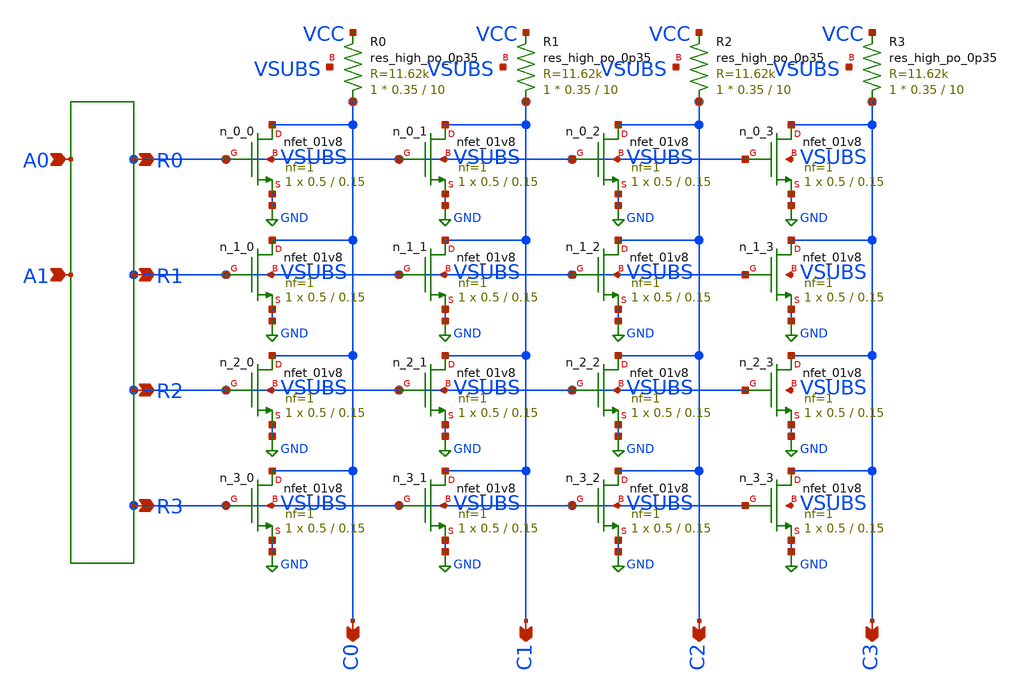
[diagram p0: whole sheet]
** sch_path: xschem/rom_4x4.sch
**.subckt rom_4x4 C0 C1 C2 C3
*.opin C0
*.opin C1
*.opin C2
*.opin C3
XR0 C0 VCC VSUBS sky130_fd_pr__res_high_po_0p35 L=10 mult=1 m=1
XR1 C1 VCC VSUBS sky130_fd_pr__res_high_po_0p35 L=10 mult=1 m=1
XR2 C2 VCC VSUBS sky130_fd_pr__res_high_po_0p35 L=10 mult=1 m=1
XR3 C3 VCC VSUBS sky130_fd_pr__res_high_po_0p35 L=10 mult=1 m=1
Xn_0_0 C0 VSUBS GND VSUBS sky130_fd_pr__nfet_01v8 L=0.15 W=0.5 nf=1 ad='int((1 + 1)/2) * 0.5 / 1 * 0.29'
+ as='int((1 + 2)/2) * 0.5 / 1 * 0.29' pd='2*int((1 + 1)/2) * (0.5 / 1 + 0.29)' ps='2*int((1 + 2)/2) * (0.5 / 1 + 0.29)'
+ nrd='0.29 / 0.5 ' nrs='0.29 / 0.5 ' sa=0 sb=0 sd=0 mult=1 m=1
Xn_0_1 C1 VSUBS GND VSUBS sky130_fd_pr__nfet_01v8 L=0.15 W=0.5 nf=1 ad='int((1 + 1)/2) * 0.5 / 1 * 0.29'
+ as='int((1 + 2)/2) * 0.5 / 1 * 0.29' pd='2*int((1 + 1)/2) * (0.5 / 1 + 0.29)' ps='2*int((1 + 2)/2) * (0.5 / 1 + 0.29)'
+ nrd='0.29 / 0.5 ' nrs='0.29 / 0.5 ' sa=0 sb=0 sd=0 mult=1 m=1
Xn_0_2 C2 VSUBS GND VSUBS sky130_fd_pr__nfet_01v8 L=0.15 W=0.5 nf=1 ad='int((1 + 1)/2) * 0.5 / 1 * 0.29'
+ as='int((1 + 2)/2) * 0.5 / 1 * 0.29' pd='2*int((1 + 1)/2) * (0.5 / 1 + 0.29)' ps='2*int((1 + 2)/2) * (0.5 / 1 + 0.29)'
+ nrd='0.29 / 0.5 ' nrs='0.29 / 0.5 ' sa=0 sb=0 sd=0 mult=1 m=1
Xn_0_3 C3 VSUBS GND VSUBS sky130_fd_pr__nfet_01v8 L=0.15 W=0.5 nf=1 ad='int((1 + 1)/2) * 0.5 / 1 * 0.29'
+ as='int((1 + 2)/2) * 0.5 / 1 * 0.29' pd='2*int((1 + 1)/2) * (0.5 / 1 + 0.29)' ps='2*int((1 + 2)/2) * (0.5 / 1 + 0.29)'
+ nrd='0.29 / 0.5 ' nrs='0.29 / 0.5 ' sa=0 sb=0 sd=0 mult=1 m=1
Xn_1_0 C0 VSUBS GND VSUBS sky130_fd_pr__nfet_01v8 L=0.15 W=0.5 nf=1 ad='int((1 + 1)/2) * 0.5 / 1 * 0.29'
+ as='int((1 + 2)/2) * 0.5 / 1 * 0.29' pd='2*int((1 + 1)/2) * (0.5 / 1 + 0.29)' ps='2*int((1 + 2)/2) * (0.5 / 1 + 0.29)'
+ nrd='0.29 / 0.5 ' nrs='0.29 / 0.5 ' sa=0 sb=0 sd=0 mult=1 m=1
Xn_1_1 C1 VSUBS GND VSUBS sky130_fd_pr__nfet_01v8 L=0.15 W=0.5 nf=1 ad='int((1 + 1)/2) * 0.5 / 1 * 0.29'
+ as='int((1 + 2)/2) * 0.5 / 1 * 0.29' pd='2*int((1 + 1)/2) * (0.5 / 1 + 0.29)' ps='2*int((1 + 2)/2) * (0.5 / 1 + 0.29)'
+ nrd='0.29 / 0.5 ' nrs='0.29 / 0.5 ' sa=0 sb=0 sd=0 mult=1 m=1
Xn_1_2 C2 VSUBS GND VSUBS sky130_fd_pr__nfet_01v8 L=0.15 W=0.5 nf=1 ad='int((1 + 1)/2) * 0.5 / 1 * 0.29'
+ as='int((1 + 2)/2) * 0.5 / 1 * 0.29' pd='2*int((1 + 1)/2) * (0.5 / 1 + 0.29)' ps='2*int((1 + 2)/2) * (0.5 / 1 + 0.29)'
+ nrd='0.29 / 0.5 ' nrs='0.29 / 0.5 ' sa=0 sb=0 sd=0 mult=1 m=1
Xn_1_3 C3 VSUBS GND VSUBS sky130_fd_pr__nfet_01v8 L=0.15 W=0.5 nf=1 ad='int((1 + 1)/2) * 0.5 / 1 * 0.29'
+ as='int((1 + 2)/2) * 0.5 / 1 * 0.29' pd='2*int((1 + 1)/2) * (0.5 / 1 + 0.29)' ps='2*int((1 + 2)/2) * (0.5 / 1 + 0.29)'
+ nrd='0.29 / 0.5 ' nrs='0.29 / 0.5 ' sa=0 sb=0 sd=0 mult=1 m=1
Xn_2_0 C0 VSUBS GND VSUBS sky130_fd_pr__nfet_01v8 L=0.15 W=0.5 nf=1 ad='int((1 + 1)/2) * 0.5 / 1 * 0.29'
+ as='int((1 + 2)/2) * 0.5 / 1 * 0.29' pd='2*int((1 + 1)/2) * (0.5 / 1 + 0.29)' ps='2*int((1 + 2)/2) * (0.5 / 1 + 0.29)'
+ nrd='0.29 / 0.5 ' nrs='0.29 / 0.5 ' sa=0 sb=0 sd=0 mult=1 m=1
Xn_2_1 C1 VSUBS GND VSUBS sky130_fd_pr__nfet_01v8 L=0.15 W=0.5 nf=1 ad='int((1 + 1)/2) * 0.5 / 1 * 0.29'
+ as='int((1 + 2)/2) * 0.5 / 1 * 0.29' pd='2*int((1 + 1)/2) * (0.5 / 1 + 0.29)' ps='2*int((1 + 2)/2) * (0.5 / 1 + 0.29)'
+ nrd='0.29 / 0.5 ' nrs='0.29 / 0.5 ' sa=0 sb=0 sd=0 mult=1 m=1
Xn_2_2 C2 VSUBS GND VSUBS sky130_fd_pr__nfet_01v8 L=0.15 W=0.5 nf=1 ad='int((1 + 1)/2) * 0.5 / 1 * 0.29'
+ as='int((1 + 2)/2) * 0.5 / 1 * 0.29' pd='2*int((1 + 1)/2) * (0.5 / 1 + 0.29)' ps='2*int((1 + 2)/2) * (0.5 / 1 + 0.29)'
+ nrd='0.29 / 0.5 ' nrs='0.29 / 0.5 ' sa=0 sb=0 sd=0 mult=1 m=1
Xn_2_3 C3 VSUBS GND VSUBS sky130_fd_pr__nfet_01v8 L=0.15 W=0.5 nf=1 ad='int((1 + 1)/2) * 0.5 / 1 * 0.29'
+ as='int((1 + 2)/2) * 0.5 / 1 * 0.29' pd='2*int((1 + 1)/2) * (0.5 / 1 + 0.29)' ps='2*int((1 + 2)/2) * (0.5 / 1 + 0.29)'
+ nrd='0.29 / 0.5 ' nrs='0.29 / 0.5 ' sa=0 sb=0 sd=0 mult=1 m=1
Xn_3_0 C0 VSUBS GND VSUBS sky130_fd_pr__nfet_01v8 L=0.15 W=0.5 nf=1 ad='int((1 + 1)/2) * 0.5 / 1 * 0.29'
+ as='int((1 + 2)/2) * 0.5 / 1 * 0.29' pd='2*int((1 + 1)/2) * (0.5 / 1 + 0.29)' ps='2*int((1 + 2)/2) * (0.5 / 1 + 0.29)'
+ nrd='0.29 / 0.5 ' nrs='0.29 / 0.5 ' sa=0 sb=0 sd=0 mult=1 m=1
Xn_3_1 C1 VSUBS GND VSUBS sky130_fd_pr__nfet_01v8 L=0.15 W=0.5 nf=1 ad='int((1 + 1)/2) * 0.5 / 1 * 0.29'
+ as='int((1 + 2)/2) * 0.5 / 1 * 0.29' pd='2*int((1 + 1)/2) * (0.5 / 1 + 0.29)' ps='2*int((1 + 2)/2) * (0.5 / 1 + 0.29)'
+ nrd='0.29 / 0.5 ' nrs='0.29 / 0.5 ' sa=0 sb=0 sd=0 mult=1 m=1
Xn_3_2 C2 VSUBS GND VSUBS sky130_fd_pr__nfet_01v8 L=0.15 W=0.5 nf=1 ad='int((1 + 1)/2) * 0.5 / 1 * 0.29'
+ as='int((1 + 2)/2) * 0.5 / 1 * 0.29' pd='2*int((1 + 1)/2) * (0.5 / 1 + 0.29)' ps='2*int((1 + 2)/2) * (0.5 / 1 + 0.29)'
+ nrd='0.29 / 0.5 ' nrs='0.29 / 0.5 ' sa=0 sb=0 sd=0 mult=1 m=1
Xn_3_3 C3 VSUBS GND VSUBS sky130_fd_pr__nfet_01v8 L=0.15 W=0.5 nf=1 ad='int((1 + 1)/2) * 0.5 / 1 * 0.29'
+ as='int((1 + 2)/2) * 0.5 / 1 * 0.29' pd='2*int((1 + 1)/2) * (0.5 / 1 + 0.29)' ps='2*int((1 + 2)/2) * (0.5 / 1 + 0.29)'
+ nrd='0.29 / 0.5 ' nrs='0.29 / 0.5 ' sa=0 sb=0 sd=0 mult=1 m=1
**.ends
.GLOBAL GND
.end
